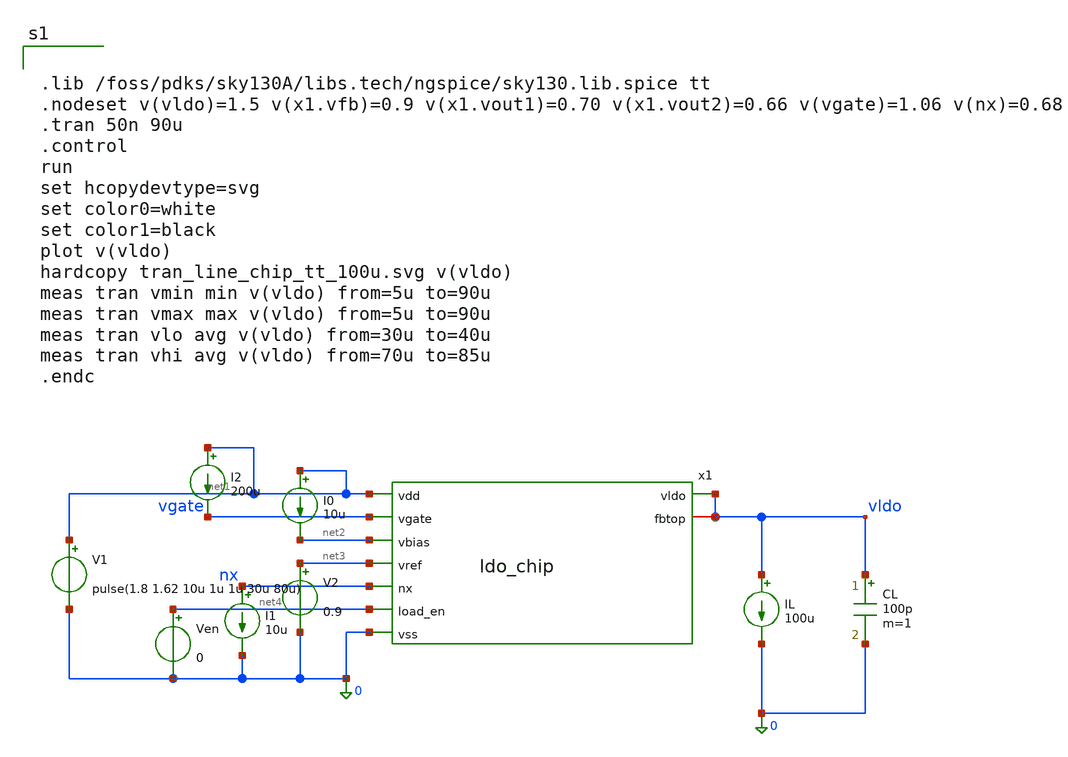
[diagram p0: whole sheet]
** sch_path: src/ldo_tran.sch
**.subckt ldo_tran
I0 net1 net2 10u
V1 net1 0 pulse(1.8 1.62 10u 1u 1u 30u 80u)
V2 net3 0 0.9
I1 nx 0 10u
I2 net1 vgate 200u
Ven net4 0 0
CL vldo 0 100p m=1
IL vldo 0 100u
x1 net1 vgate net2 net3 vldo vldo nx net4 0 ldo_chip
**** begin user architecture code


.lib /foss/pdks/sky130A/libs.tech/ngspice/sky130.lib.spice tt
.nodeset v(vldo)=1.5 v(x1.vfb)=0.9 v(x1.vout1)=0.70 v(x1.vout2)=0.66 v(vgate)=1.06 v(nx)=0.68
.tran 50n 90u
.control
run
set hcopydevtype=svg
set color0=white
set color1=black
plot v(vldo)
hardcopy tran_line_chip_tt_100u.svg v(vldo)
meas tran vmin min v(vldo) from=5u to=90u
meas tran vmax max v(vldo) from=5u to=90u
meas tran vlo avg v(vldo) from=30u to=40u
meas tran vhi avg v(vldo) from=70u to=85u
.endc


**** end user architecture code
**.ends

* expanding   symbol:  /foss/designs/ldo_project/ldo_chip.sym # of pins=9
** sym_path: src/ldo_chip.sym
** sch_path: src/ldo_chip.sch
.subckt ldo_chip vdd vgate vbias vref vldo fbtop nx load_en vss
*.ipin vdd
*.ipin vss
*.ipin vref
*.opin vldo
*.ipin load_en
*.iopin fbtop
*.ipin vbias
*.ipin nx
*.ipin vgate
XM1 net1 vref net2 vss sky130_fd_pr__nfet_01v8 L=0.5 W=10 nf=1 ad='int((1 + 1)/2) * 10 / 1 * 0.29' as='int((1 + 2)/2) * 10 / 1 * 0.29'
+ pd='2*int((1 + 1)/2) * (10 / 1 + 0.29)' ps='2*int((1 + 2)/2) * (10 / 1 + 0.29)' nrd='0.29 / 10 ' nrs='0.29 / 10 '
+ sa=0 sb=0 sd=0 mult=1 m=1
XM2 vout1 vfb net2 vss sky130_fd_pr__nfet_01v8 L=0.5 W=10 nf=1 ad='int((1 + 1)/2) * 10 / 1 * 0.29' as='int((1 + 2)/2) * 10 / 1 * 0.29'
+ pd='2*int((1 + 1)/2) * (10 / 1 + 0.29)' ps='2*int((1 + 2)/2) * (10 / 1 + 0.29)' nrd='0.29 / 10 ' nrs='0.29 / 10 '
+ sa=0 sb=0 sd=0 mult=1 m=1
XM3 net1 net1 vdd vdd sky130_fd_pr__pfet_01v8 L=0.5 W=5 nf=1 ad='int((1 + 1)/2) * 5 / 1 * 0.29' as='int((1 + 2)/2) * 5 / 1 * 0.29'
+ pd='2*int((1 + 1)/2) * (5 / 1 + 0.29)' ps='2*int((1 + 2)/2) * (5 / 1 + 0.29)' nrd='0.29 / 5 ' nrs='0.29 / 5 '
+ sa=0 sb=0 sd=0 mult=1 m=1
XM4 vout1 net1 vdd vdd sky130_fd_pr__pfet_01v8 L=0.5 W=5 nf=1 ad='int((1 + 1)/2) * 5 / 1 * 0.29' as='int((1 + 2)/2) * 5 / 1 * 0.29'
+ pd='2*int((1 + 1)/2) * (5 / 1 + 0.29)' ps='2*int((1 + 2)/2) * (5 / 1 + 0.29)' nrd='0.29 / 5 ' nrs='0.29 / 5 '
+ sa=0 sb=0 sd=0 mult=1 m=1
XM5 net2 vbias vss vss sky130_fd_pr__nfet_01v8 L=1 W=5 nf=1 ad='int((1 + 1)/2) * 5 / 1 * 0.29' as='int((1 + 2)/2) * 5 / 1 * 0.29'
+ pd='2*int((1 + 1)/2) * (5 / 1 + 0.29)' ps='2*int((1 + 2)/2) * (5 / 1 + 0.29)' nrd='0.29 / 5 ' nrs='0.29 / 5 '
+ sa=0 sb=0 sd=0 mult=1 m=1
XM6 vbias vbias vss vss sky130_fd_pr__nfet_01v8 L=1 W=5 nf=1 ad='int((1 + 1)/2) * 5 / 1 * 0.29' as='int((1 + 2)/2) * 5 / 1 * 0.29'
+ pd='2*int((1 + 1)/2) * (5 / 1 + 0.29)' ps='2*int((1 + 2)/2) * (5 / 1 + 0.29)' nrd='0.29 / 5 ' nrs='0.29 / 5 '
+ sa=0 sb=0 sd=0 mult=1 m=1
XM7 vout2 vout1 vdd vdd sky130_fd_pr__pfet_01v8 L=0.5 W=60 nf=1 ad='int((1 + 1)/2) * 60 / 1 * 0.29' as='int((1 + 2)/2) * 60 / 1 * 0.29'
+ pd='2*int((1 + 1)/2) * (60 / 1 + 0.29)' ps='2*int((1 + 2)/2) * (60 / 1 + 0.29)' nrd='0.29 / 60 ' nrs='0.29 / 60 '
+ sa=0 sb=0 sd=0 mult=1 m=1
XM8 vout2 vbias vss vss sky130_fd_pr__nfet_01v8 L=1 W=30 nf=1 ad='int((1 + 1)/2) * 30 / 1 * 0.29' as='int((1 + 2)/2) * 30 / 1 * 0.29'
+ pd='2*int((1 + 1)/2) * (30 / 1 + 0.29)' ps='2*int((1 + 2)/2) * (30 / 1 + 0.29)' nrd='0.29 / 30 ' nrs='0.29 / 30 '
+ sa=0 sb=0 sd=0 mult=1 m=1
XMp vldo vgate vdd vdd sky130_fd_pr__pfet_01v8 L=0.15 W=2000 nf=400 ad='int((400 + 1)/2) * 2000 / 400 * 0.29'
+ as='int((400 + 2)/2) * 2000 / 400 * 0.29' pd='2*int((400 + 1)/2) * (2000 / 400 + 0.29)' ps='2*int((400 + 2)/2) * (2000 / 400 + 0.29)'
+ nrd='0.29 / 2000 ' nrs='0.29 / 2000 ' sa=0 sb=0 sd=0 mult=1 m=1
XMb2 vgate nx vss vss sky130_fd_pr__nfet_01v8 L=0.5 W=100 nf=20 ad='int((20 + 1)/2) * 100 / 20 * 0.29'
+ as='int((20 + 2)/2) * 100 / 20 * 0.29' pd='2*int((20 + 1)/2) * (100 / 20 + 0.29)' ps='2*int((20 + 2)/2) * (100 / 20 + 0.29)'
+ nrd='0.29 / 100 ' nrs='0.29 / 100 ' sa=0 sb=0 sd=0 mult=1 m=1
XMb1 nx vout2 vgate vgate sky130_fd_pr__pfet_01v8_lvt L=0.5 W=50 nf=10 ad='int((10 + 1)/2) * 50 / 10 * 0.29'
+ as='int((10 + 2)/2) * 50 / 10 * 0.29' pd='2*int((10 + 1)/2) * (50 / 10 + 0.29)' ps='2*int((10 + 2)/2) * (50 / 10 + 0.29)'
+ nrd='0.29 / 50 ' nrs='0.29 / 50 ' sa=0 sb=0 sd=0 mult=1 m=1
XMsw nsw load_en vss vss sky130_fd_pr__nfet_01v8 L=0.5 W=30 nf=6 ad='int((6 + 1)/2) * 30 / 6 * 0.29'
+ as='int((6 + 2)/2) * 30 / 6 * 0.29' pd='2*int((6 + 1)/2) * (30 / 6 + 0.29)' ps='2*int((6 + 2)/2) * (30 / 6 + 0.29)'
+ nrd='0.29 / 30 ' nrs='0.29 / 30 ' sa=0 sb=0 sd=0 mult=1 m=1
XRload nsw vldo vss sky130_fd_pr__res_high_po W=1 L=0.6 mult=1 m=1
XCM1 net3 vout1 sky130_fd_pr__cap_mim_m3_1 W=20 L=25 MF=11 m=11
XCM2 net3 vout1 sky130_fd_pr__cap_mim_m3_2 W=20 L=25 MF=11 m=11
XRZ vout2 net3 vss sky130_fd_pr__res_high_po W=0.69 L=1.2 mult=1 m=1
XRbl vss vldo vss sky130_fd_pr__res_high_po W=2.85 L=12.3 mult=1 m=1
XRf1 vfb fbtop vss sky130_fd_pr__res_xhigh_po W=0.35 L=35 mult=1 m=1
XRf2 vss vfb vss sky130_fd_pr__res_xhigh_po W=0.35 L=52.5 mult=1 m=1
.ends

.end
